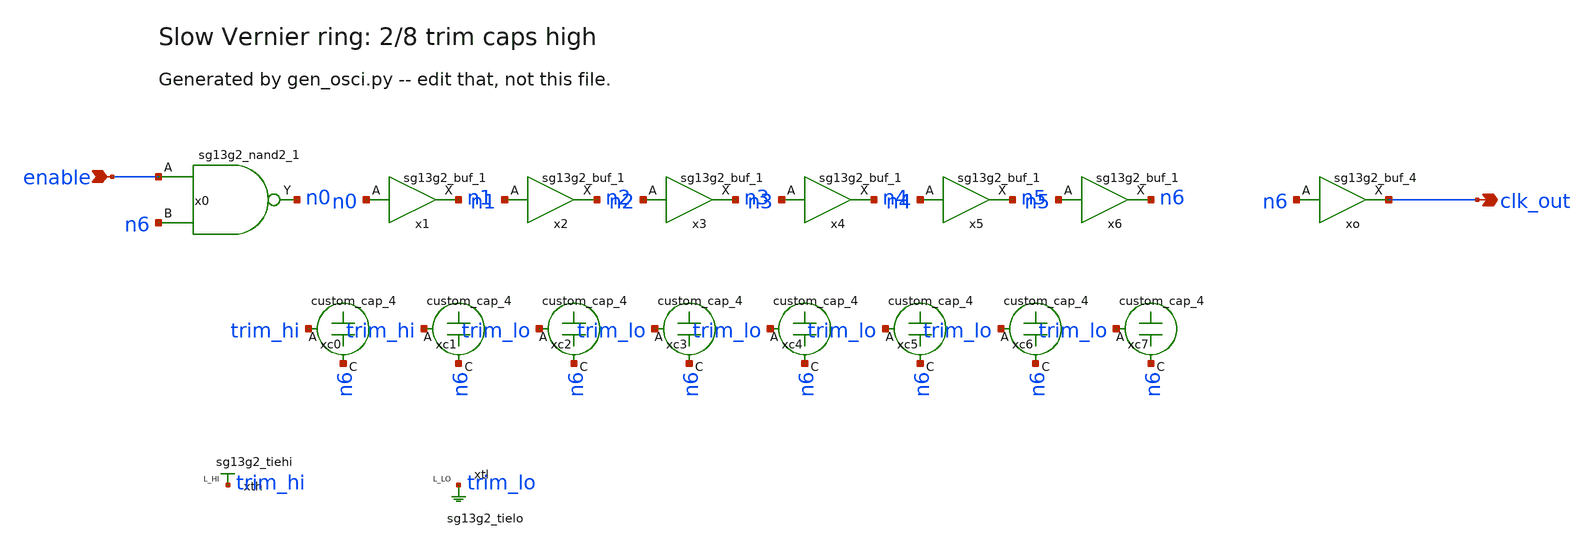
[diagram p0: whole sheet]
** sch_path: TPU5555-main/mdll/mixed_signal_design_blocks/tdc/osci/src/slow_osci.sch
* IHP-GmbH/IHP-Open-PDK/ihp-sg13g2/libs.tech/xschem/sg13g2_stdcells/sg13g2_buf_1.sch:
* Copyright 2023 IHP PDK Authors
* Licensed under the Apache License, Version 2.0 (the "License");
**.subckt slow_osci enable clk_out
*.ipin enable
*.opin clk_out
x0 n0 enable n6 VDD VSS sg13g2_nand2_1
x1 n1 n0 VDD VSS sg13g2_buf_1
x2 n2 n1 VDD VSS sg13g2_buf_1
x3 n3 n2 VDD VSS sg13g2_buf_1
x4 n4 n3 VDD VSS sg13g2_buf_1
x5 n5 n4 VDD VSS sg13g2_buf_1
x6 n6 n5 VDD VSS sg13g2_buf_1
xo clk_out n6 VDD VSS sg13g2_buf_4
xc0 n6 trim_hi VDD VSS custom_cap_4
xc1 n6 trim_hi VDD VSS custom_cap_4
xc2 n6 trim_lo VDD VSS custom_cap_4
xc3 n6 trim_lo VDD VSS custom_cap_4
xc4 n6 trim_lo VDD VSS custom_cap_4
xc5 n6 trim_lo VDD VSS custom_cap_4
xc6 n6 trim_lo VDD VSS custom_cap_4
xc7 n6 trim_lo VDD VSS custom_cap_4
xth trim_hi VDD VSS sg13g2_tiehi
xtl trim_lo VDD VSS sg13g2_tielo
**.ends

* expanding   symbol:  sg13g2_nand2_1.sym # of pins=3
** sym_path: sg13g2_nand2_1.sym
** sch_path: sg13g2_nand2_1.sch
.subckt sg13g2_nand2_1 Y A B VDD VSS
*.iopin VDD
*.iopin VSS
*.ipin A
*.ipin B
*.opin Y
XM1 Y A net1 VSS sg13_lv_nmos w=740.00n l=130.00n ng=1 m=1 mm_ok=1
XM2 net1 B VSS VSS sg13_lv_nmos w=740.00n l=130.00n ng=1 m=1 mm_ok=1
XM3 Y A VDD VDD sg13_lv_pmos w=1.12u l=130.00n ng=1 m=1 mm_ok=1
XM4 Y B VDD VDD sg13_lv_pmos w=1.12u l=130.00n ng=1 m=1 mm_ok=1
.ends


* expanding   symbol:  sg13g2_buf_1.sym # of pins=2
** sym_path: sg13g2_buf_1.sym
** sch_path: sg13g2_buf_1.sch
.subckt sg13g2_buf_1 X A VDD VSS
*.ipin A
*.opin X
*.iopin VDD
*.iopin VSS
XM1 net1 A VSS VSS sg13_lv_nmos w=550.00n l=130.00n ng=1 m=1 mm_ok=1
XM2 X net1 VSS VSS sg13_lv_nmos w=740.00n l=130.00n ng=1 m=1 mm_ok=1
XM3 net1 A VDD VDD sg13_lv_pmos w=840.00n l=130.00n ng=1 m=1 mm_ok=1
XM4 X net1 VDD VDD sg13_lv_pmos w=1.12u l=130.00n ng=1 m=1 mm_ok=1
.ends


* expanding   symbol:  sg13g2_buf_4.sym # of pins=2
** sym_path: sg13g2_buf_4.sym
** sch_path: sg13g2_buf_4.sch
.subckt sg13g2_buf_4 X A VDD VSS
*.ipin A
*.opin X
*.iopin VDD
*.iopin VSS
XM1 net1 A VSS VSS sg13_lv_nmos w=740.00n l=130.00n ng=1 m=1 mm_ok=1
XM2 X net1 VSS VSS sg13_lv_nmos w=2.96u l=130.00n ng=4 m=1 mm_ok=1
XM3 net1 A VDD VDD sg13_lv_pmos w=1.68u l=130.00n ng=2 m=1 mm_ok=1
XM4 X net1 VDD VDD sg13_lv_pmos w=4.48u l=130.00n ng=4 m=1 mm_ok=1
.ends

.end
